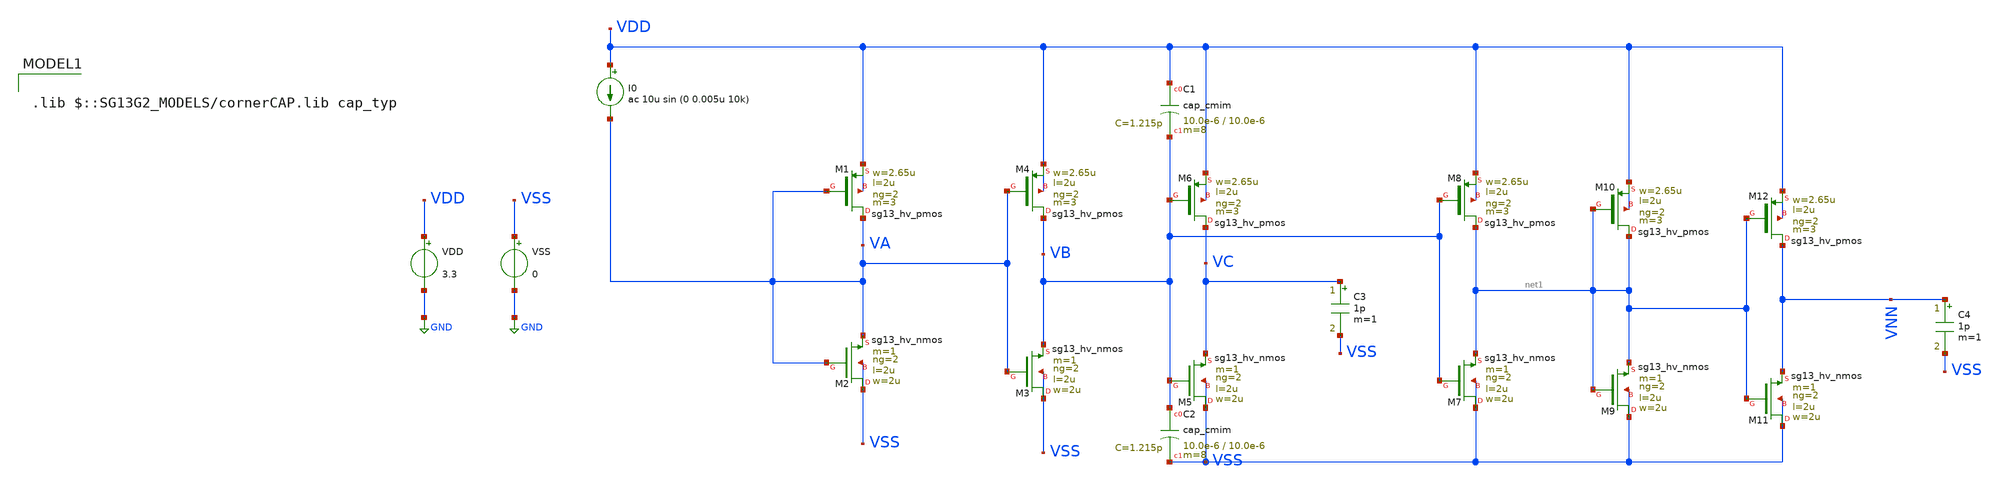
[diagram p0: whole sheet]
** sch_path: Learning/curr_amplifiers/CA001_ihp_3_3V/tb.sch
**.subckt tb
VDD VDD GND 3.3
VSS VSS GND 0
I0 VDD VA ac 10u sin (0 0.005u 10k)
XM1 VA VA VDD VDD sg13_hv_pmos w=2.65u l=2u ng=2 m=3 mm_ok=1
XM2 VSS VA VA VSS sg13_hv_nmos w=2u l=2u ng=2 m=1 mm_ok=1
XM3 VSS VA VB VSS sg13_hv_nmos w=2u l=2u ng=2 m=1 mm_ok=1
XM4 VB VA VDD VDD sg13_hv_pmos w=2.65u l=2u ng=2 m=3 mm_ok=1
XM5 VSS VB VC VSS sg13_hv_nmos w=2u l=2u ng=2 m=1 mm_ok=1
XM6 VC VB VDD VDD sg13_hv_pmos w=2.65u l=2u ng=2 m=3 mm_ok=1
XC1 VDD VB cap_cmim w=10.0e-6 l=10.0e-6 m=8 mm_ok=1
C3 VC VSS 1p m=1
XC2 VB VSS cap_cmim w=10.0e-6 l=10.0e-6 m=8 mm_ok=1
XM7 VSS VB net1 VSS sg13_hv_nmos w=2u l=2u ng=2 m=1 mm_ok=1
XM8 net1 VB VDD VDD sg13_hv_pmos w=2.65u l=2u ng=2 m=3 mm_ok=1
XM9 VSS net1 net1 VSS sg13_hv_nmos w=2u l=2u ng=2 m=1 mm_ok=1
XM10 net1 net1 VDD VDD sg13_hv_pmos w=2.65u l=2u ng=2 m=3 mm_ok=1
XM11 VSS net1 VNN VSS sg13_hv_nmos w=2u l=2u ng=2 m=1 mm_ok=1
XM12 VNN net1 VDD VDD sg13_hv_pmos w=2.65u l=2u ng=2 m=3 mm_ok=1
C4 VNN VSS 1p m=1
**** begin user architecture code

.lib cornerMOShv.lib mos_tt


.lib $::SG13G2_MODELS/cornerCAP.lib cap_typ



.param temp=27
.param mm_ok=0
.param mc_ok=0
.control
	save all
	dc I0 -50u 50u 0.1u
	plot v(VA)
	plot i(VDD)
	plot v(VC)
	ac dec 100 1 10G
	plot db(v(VC)) (180*ph(v(VC))/pi)
	plot db(v(VNN)) (180*ph(v(VNN))/pi)
	tran 10ns 1m
	plot v(VC) v(VNN)
	plot i(VSS)

.endc


**** end user architecture code
**.ends
.GLOBAL GND
.end
